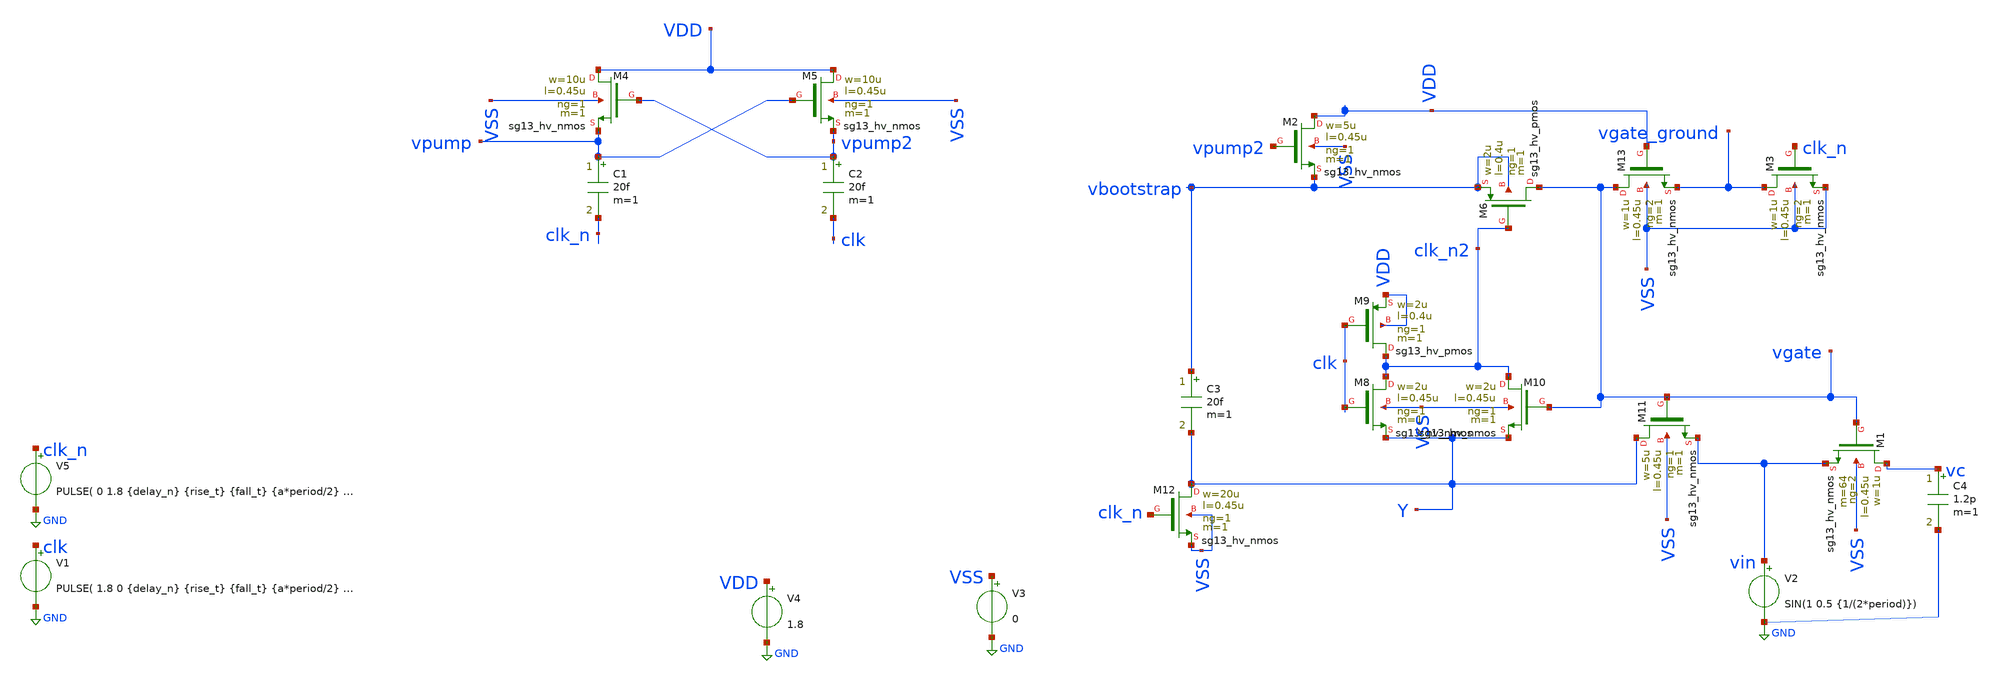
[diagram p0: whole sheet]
** sch_path: xschem/bootstrap/tb_bootstrap.sch
**.subckt tb_bootstrap
V2 vin GND SIN(1 0.5 {1/(2*period)})
V4 VDD GND 1.8
C1 vpump clk_n 20f m=1
C2 vpump2 clk 20f m=1
XM6 vgate clk_n2 vbootstrap vbootstrap sg13_hv_pmos w=2u l=0.4u ng=1 m=1 mm_ok=1
XM8 clk_n2 clk Y VSS sg13_hv_nmos w=2u l=0.45u ng=1 m=1 mm_ok=1
XM9 clk_n2 clk VDD VDD sg13_hv_pmos w=2u l=0.4u ng=1 m=1 mm_ok=1
XM10 clk_n2 vgate Y VSS sg13_hv_nmos w=2u l=0.45u ng=1 m=1 mm_ok=1
XM11 Y vgate vin VSS sg13_hv_nmos w=5u l=0.45u ng=1 m=1 mm_ok=1
C3 vbootstrap Y 20f m=1
XM12 Y clk_n VSS VSS sg13_hv_nmos w=20u l=0.45u ng=1 m=1 mm_ok=1
XM13 vgate VDD vgate_ground VSS sg13_hv_nmos w=1u l=0.45u ng=2 m=1 mm_ok=1
XM3 vgate_ground clk_n VSS VSS sg13_hv_nmos w=1u l=0.45u ng=2 m=1 mm_ok=1
XM4 VDD vpump2 vpump VSS sg13_hv_nmos w=10u l=0.45u ng=1 m=1 mm_ok=1
XM5 VDD vpump vpump2 VSS sg13_hv_nmos w=10u l=0.45u ng=1 m=1 mm_ok=1
XM1 vc vgate vin VSS sg13_hv_nmos w=1u l=0.45u ng=2 m=64 mm_ok=1
V1 clk GND PULSE( 1.8 0 {delay_n} {rise_t} {fall_t} {a*period/2} {a*period} )
V5 clk_n GND PULSE( 0 1.8 {delay_n} {rise_t} {fall_t} {a*period/2} {a*period} )
C4 vc GND 1.2p m=1
V3 VSS GND 0
XM2 VDD vpump2 vbootstrap VSS sg13_hv_nmos w=5u l=0.45u ng=1 m=1 mm_ok=1
**** begin user architecture code


.param temp=27
.param period = 1n
.param wp = 1.5u
.param a = 1.8
.param wn = 0.5u
.param rise_t = period*0.1
.param fall_t = period*0.1
.param delay_n = 0
.param delay_s = 10p
.param delay_2 = period*0.2
.param delay_1 = 0
.options savecurrents klu method=gear reltol=1e-2 abstol=1e-15 gmin=1e-10
.control

* Transient Analysis
tran 1p 10n

plot clk clk_n vpump vpump2
plot vin vgate vc
plot vbootstrap vgate_ground  vgate Y clk clk_n clk_n2
.endc




** IHP models
.lib cornerMOSlv.lib mos_tt
.lib cornerMOShv.lib mos_tt
.lib cornerHBT.lib hbt_typ
.lib cornerRES.lib res_typ
.include /foss/pdks/ihp-sg13g2/libs.ref/sg13g2_stdcell/spice/sg13g2_stdcell.spice


**** end user architecture code
**.ends
.GLOBAL GND
.end
